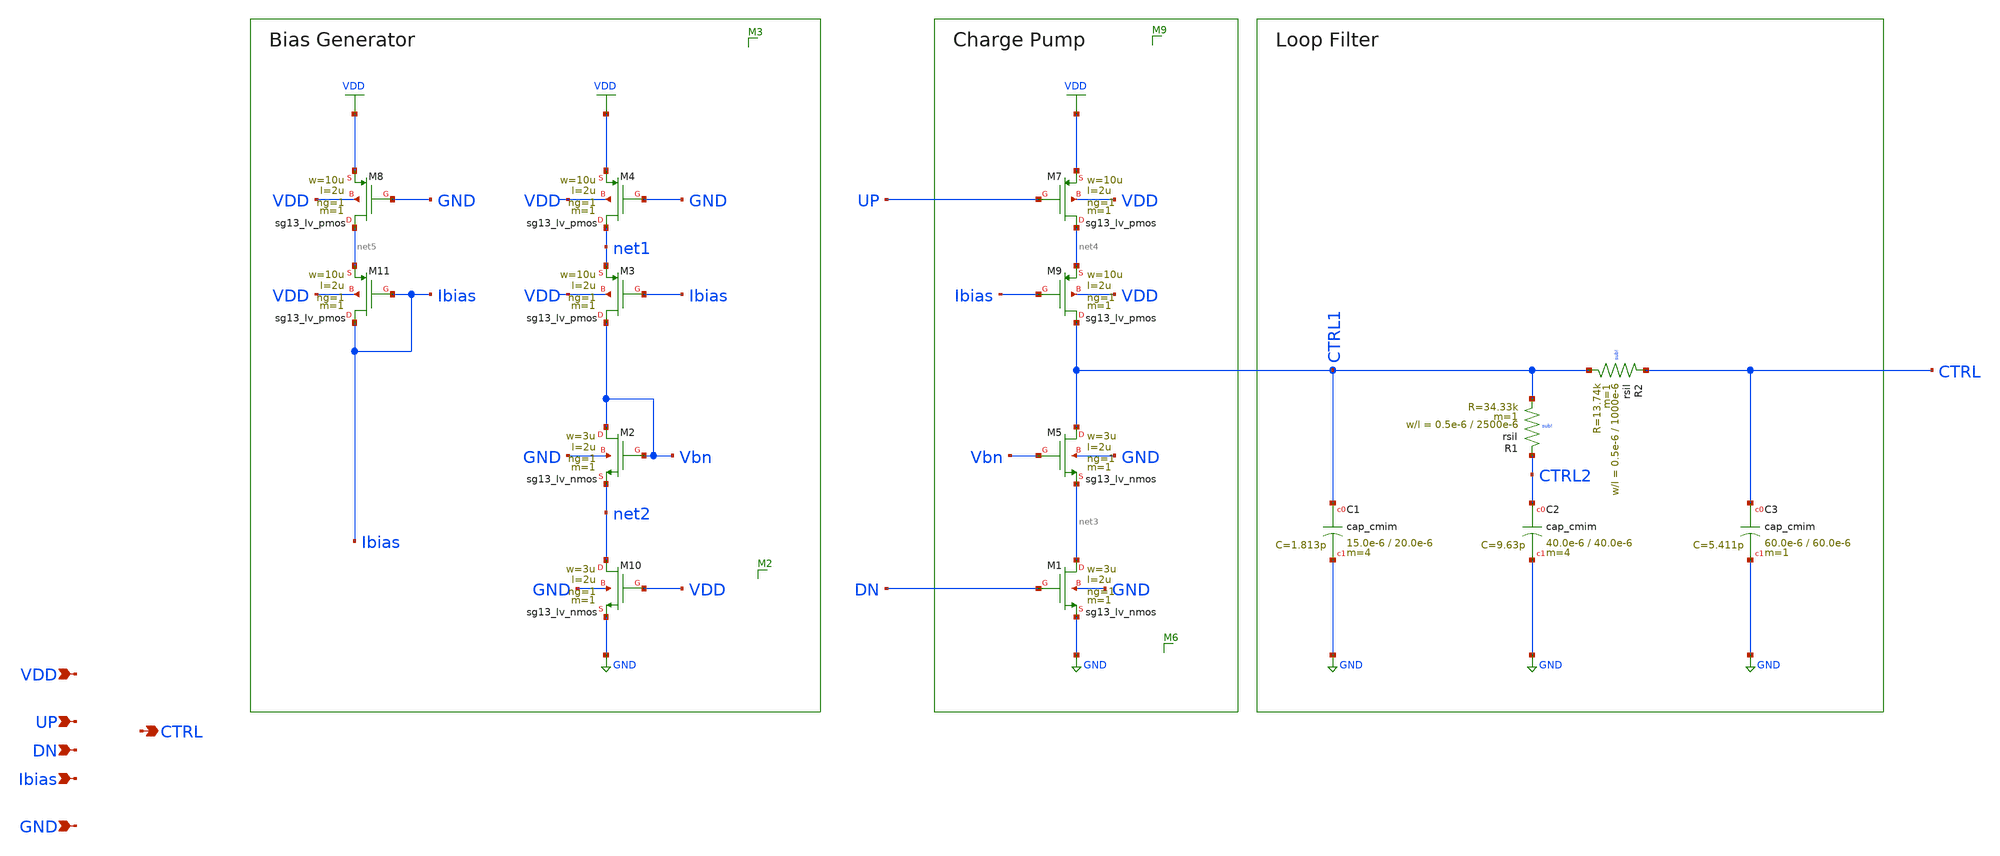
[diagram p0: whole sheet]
** sch_path: schematic/charge-pump/CP1.sch
**.subckt CP1 CTRL UP VDD Ibias DN GND
*.opin CTRL
*.ipin UP
*.ipin VDD
*.ipin Ibias
*.ipin DN
*.ipin GND
XM2 Vbn Vbn net2 GND sg13_lv_nmos w=3u l=2u ng=1 m=1 mm_ok=1
XM8 net5 GND VDD VDD sg13_lv_pmos w=10u l=2u ng=1 m=1 mm_ok=1
XR2 CTRL CTRL1 sub! rsil w=0.5e-6 l=1000e-6 m=1 mm_ok=1
XR1 CTRL2 CTRL1 sub! rsil w=0.5e-6 l=2500e-6 m=1 mm_ok=1
XC3 CTRL GND cap_cmim w=60.0e-6 l=60.0e-6 m=1 mm_ok=1
XC2 CTRL2 GND cap_cmim w=40.0e-6 l=40.0e-6 m=4 mm_ok=1
XC1 CTRL1 GND cap_cmim w=15.0e-6 l=20.0e-6 m=4 mm_ok=1
XM11 Ibias Ibias net5 VDD sg13_lv_pmos w=10u l=2u ng=1 m=1 mm_ok=1
XM3 Vbn Ibias net1 VDD sg13_lv_pmos w=10u l=2u ng=1 m=1 mm_ok=1
XM4 net1 GND VDD VDD sg13_lv_pmos w=10u l=2u ng=1 m=1 mm_ok=1
XM7 net4 UP VDD VDD sg13_lv_pmos w=10u l=2u ng=1 m=1 mm_ok=1
XM9 CTRL1 Ibias net4 VDD sg13_lv_pmos w=10u l=2u ng=1 m=1 mm_ok=1
XM10 net2 VDD GND GND sg13_lv_nmos w=3u l=2u ng=1 m=1 mm_ok=1
XM1 net3 DN GND GND sg13_lv_nmos w=3u l=2u ng=1 m=1 mm_ok=1
XM5 CTRL1 Vbn net3 GND sg13_lv_nmos w=3u l=2u ng=1 m=1 mm_ok=1
**.ends
.GLOBAL GND
.GLOBAL VDD
.end
